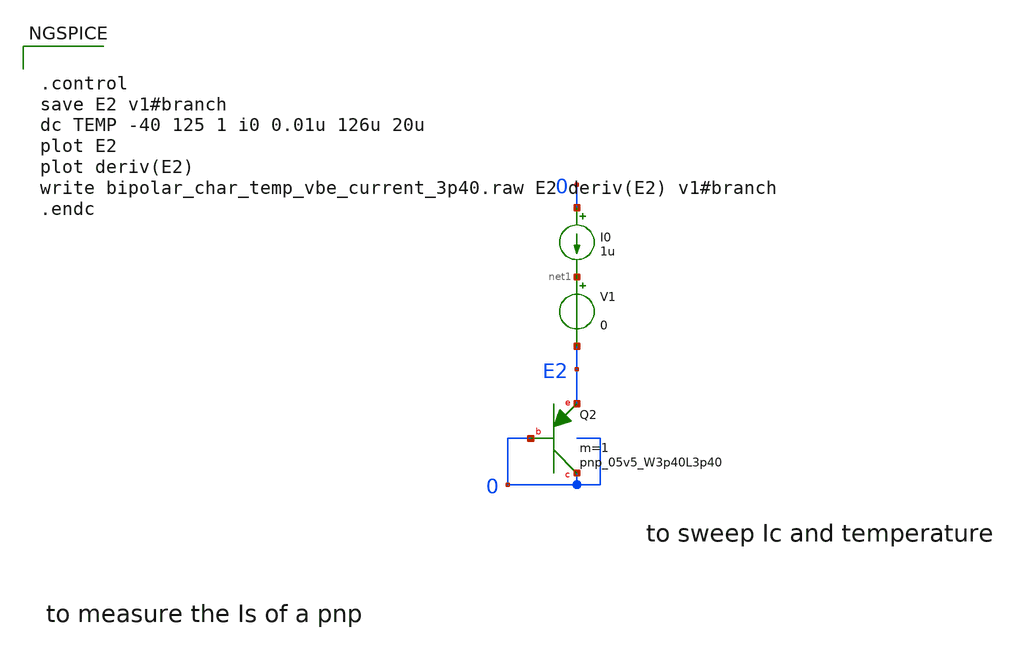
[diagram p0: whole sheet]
** sch_path: schematics/bipolar_characterization_temp_and_vbe_3p40.sch
**.subckt bipolar_characterization_temp_and_vbe_3p40
XQ2 0 0 E2 sky130_fd_pr__pnp_05v5_W3p40L3p40 m=1
I0 0 net1 1u
V1 net1 E2 0
**** begin user architecture code


.control
save E2 v1#branch
dc TEMP -40 125 1 i0 0.01u 126u 20u
plot E2
plot deriv(E2)
write bipolar_char_temp_vbe_current_3p40.raw E2 deriv(E2) v1#branch
.endc



.include $::SKYWATER_MODELS/cells/nfet_01v8/sky130_fd_pr__nfet_01v8__tt.corner.spice
.include $::SKYWATER_MODELS/cells/nfet_01v8_lvt/sky130_fd_pr__nfet_01v8_lvt__tt.corner.spice
.include $::SKYWATER_MODELS/cells/pfet_01v8/sky130_fd_pr__pfet_01v8__tt.corner.spice
.include $::SKYWATER_MODELS/cells/nfet_03v3_nvt/sky130_fd_pr__nfet_03v3_nvt__tt.corner.spice
.include $::SKYWATER_MODELS/cells/nfet_05v0_nvt/sky130_fd_pr__nfet_05v0_nvt__tt.corner.spice
.include $::SKYWATER_MODELS/cells/esd_nfet_01v8/sky130_fd_pr__esd_nfet_01v8__tt.corner.spice
.include $::SKYWATER_MODELS/cells/pfet_01v8_lvt/sky130_fd_pr__pfet_01v8_lvt__tt.corner.spice
.include $::SKYWATER_MODELS/cells/pfet_01v8_hvt/sky130_fd_pr__pfet_01v8_hvt__tt.corner.spice
.include $::SKYWATER_MODELS/cells/esd_pfet_g5v0d10v5/sky130_fd_pr__esd_pfet_g5v0d10v5__tt.corner.spice
.include $::SKYWATER_MODELS/cells/pfet_g5v0d10v5/sky130_fd_pr__pfet_g5v0d10v5__tt.corner.spice
.include $::SKYWATER_MODELS/cells/pfet_g5v0d16v0/sky130_fd_pr__pfet_g5v0d16v0__tt.corner.spice
.include $::SKYWATER_MODELS/cells/nfet_g5v0d10v5/sky130_fd_pr__nfet_g5v0d10v5__tt.corner.spice
.include $::SKYWATER_MODELS/cells/nfet_g5v0d16v0/sky130_fd_pr__nfet_g5v0d16v0__tt_discrete.corner.spice
.include $::SKYWATER_MODELS/cells/esd_nfet_g5v0d10v5/sky130_fd_pr__esd_nfet_g5v0d10v5__tt.corner.spice
.include $::SKYWATER_MODELS/models/corners/tt/nonfet.spice
* Mismatch parameters
.include $::SKYWATER_MODELS/cells/nfet_01v8/sky130_fd_pr__nfet_01v8__mismatch.corner.spice
.include $::SKYWATER_MODELS/cells/pfet_01v8/sky130_fd_pr__pfet_01v8__mismatch.corner.spice
.include $::SKYWATER_MODELS/cells/nfet_01v8_lvt/sky130_fd_pr__nfet_01v8_lvt__mismatch.corner.spice
.include $::SKYWATER_MODELS/cells/pfet_01v8_lvt/sky130_fd_pr__pfet_01v8_lvt__mismatch.corner.spice
.include $::SKYWATER_MODELS/cells/pfet_01v8_hvt/sky130_fd_pr__pfet_01v8_hvt__mismatch.corner.spice
.include $::SKYWATER_MODELS/cells/nfet_g5v0d10v5/sky130_fd_pr__nfet_g5v0d10v5__mismatch.corner.spice
.include $::SKYWATER_MODELS/cells/pfet_g5v0d10v5/sky130_fd_pr__pfet_g5v0d10v5__mismatch.corner.spice
.include $::SKYWATER_MODELS/cells/nfet_05v0_nvt/sky130_fd_pr__nfet_05v0_nvt__mismatch.corner.spice
.include $::SKYWATER_MODELS/cells/nfet_03v3_nvt/sky130_fd_pr__nfet_03v3_nvt__mismatch.corner.spice
* Resistor$::SKYWATER_MODELS/Capacitor
.include $::SKYWATER_MODELS/models/r+c/res_typical__cap_typical.spice
.include $::SKYWATER_MODELS/models/r+c/res_typical__cap_typical__lin.spice
* Special cells/
.include $::SKYWATER_MODELS/models/corners/tt/specialized_cells.spice
* All models
.include $::SKYWATER_MODELS/models/all.spice
.include $::SKYWATER_MODELS/cells/pnp_05v5/sky130_fd_pr__pnp_05v5_W3p40L3p40.model.spice
* Corner
.include $::SKYWATER_MODELS/models/corners/tt/rf.spice

**** end user architecture code
**.ends
.end
